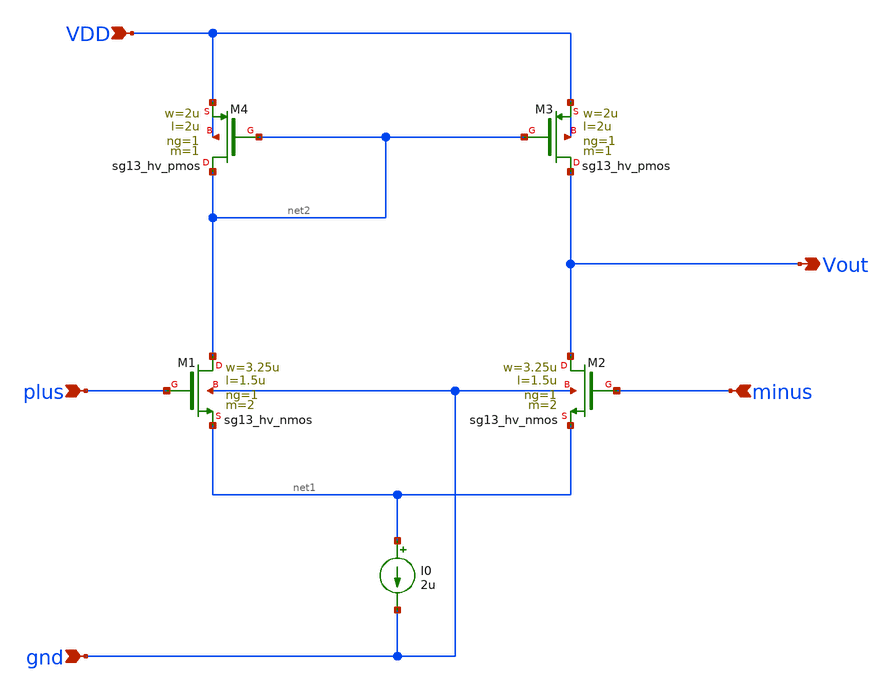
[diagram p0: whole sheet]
** sch_path: Design Files/RAMP/OTA/NOTA3.sch
**.subckt NOTA3 plus minus VDD gnd Vout
*.ipin plus
*.ipin minus
*.ipin VDD
*.ipin gnd
*.opin Vout
XM1 net2 plus net1 gnd sg13_hv_nmos w=3.25u l=1.5u ng=1 m=2 mm_ok=1
XM2 Vout minus net1 gnd sg13_hv_nmos w=3.25u l=1.5u ng=1 m=2 mm_ok=1
XM3 Vout net2 VDD VDD sg13_hv_pmos w=2u l=2u ng=1 m=1 mm_ok=1
XM4 net2 net2 VDD VDD sg13_hv_pmos w=2u l=2u ng=1 m=1 mm_ok=1
I0 net1 gnd 2u
**.ends
.end
